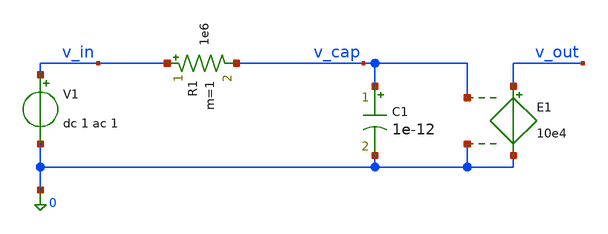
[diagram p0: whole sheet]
** sch_path: tests/xschem/xschem_tb_gain_ac.sch
**.subckt xschem_tb_gain_ac
C1 v_cap 0 1e-12 m=1
R1 v_in v_cap 1e6 m=1
V1 v_in 0 dc 1 ac 1
E1 v_out 0 v_cap 0 10e4
**.ends
.end
